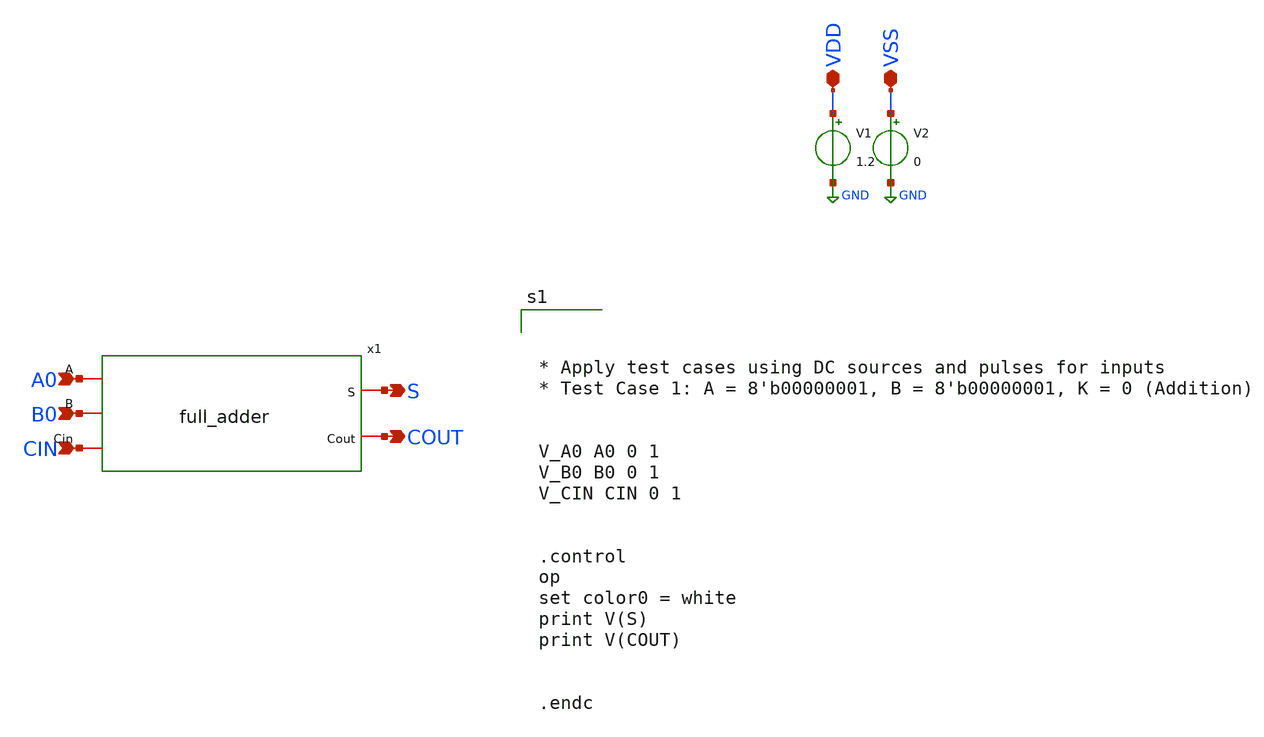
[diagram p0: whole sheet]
** sch_path: design/xschem/TEST_BENCHES/full_adder_TB.sch
**.subckt full_adder_TB VDD VSS A0 B0 CIN S COUT
*.iopin VDD
*.iopin VSS
*.ipin A0
*.ipin B0
*.ipin CIN
*.opin S
*.opin COUT
x1 A0 S B0 CIN COUT full_adder
V1 VDD GND 1.2
V2 VSS GND 0
**** begin user architecture code

** opencircuitdesign pdks install
.lib $::SKYWATER_MODELS/sky130.lib.spice tt_mm





* Apply test cases using DC sources and pulses for inputs
* Test Case 1: A = 8'b00000001, B = 8'b00000001, K = 0 (Addition)


V_A0 A0 0 1
V_B0 B0 0 1
V_CIN CIN 0 1


.control
op
set color0 = white
print V(S)
print V(COUT)


.endc


**** end user architecture code
**.ends
.GLOBAL GND
.end
